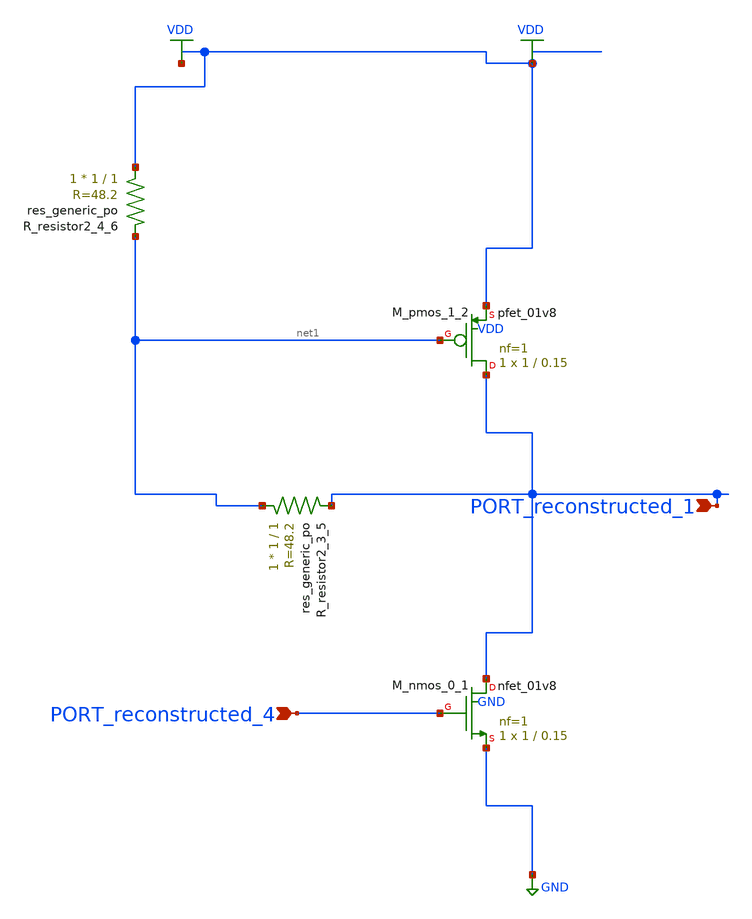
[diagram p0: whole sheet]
** sch_path: schematics/AMSNet/153.sch
**.subckt 153 PORT_reconstructed_1 PORT_reconstructed_4
*.ipin PORT_reconstructed_1
*.ipin PORT_reconstructed_4
XM_nmos_0_1 PORT_reconstructed_1 PORT_reconstructed_4 GND GND sky130_fd_pr__nfet_01v8 L=0.15 W=1 nf=1
+ ad='int((1 + 1)/2) * 1 / 1 * 0.29' as='int((1 + 2)/2) * 1 / 1 * 0.29' pd='2*int((1 + 1)/2) * (1 / 1 + 0.29)'
+ ps='2*int((1 + 2)/2) * (1 / 1 + 0.29)' nrd='0.29 / 1 ' nrs='0.29 / 1 ' sa=0 sb=0 sd=0 mult=1 m=1
XM_pmos_1_2 PORT_reconstructed_1 net1 VDD VDD sky130_fd_pr__pfet_01v8 L=0.15 W=1 nf=1 ad='int((1 + 1)/2) * 1 / 1 * 0.29'
+ as='int((1 + 2)/2) * 1 / 1 * 0.29' pd='2*int((1 + 1)/2) * (1 / 1 + 0.29)' ps='2*int((1 + 2)/2) * (1 / 1 + 0.29)'
+ nrd='0.29 / 1 ' nrs='0.29 / 1 ' sa=0 sb=0 sd=0 mult=1 m=1
XR_resistor2_3_5 net1 PORT_reconstructed_1 sky130_fd_pr__res_generic_po W=1 L=1 m=1
XR_resistor2_4_6 VDD net1 sky130_fd_pr__res_generic_po W=1 L=1 m=1
**.ends
.GLOBAL GND
.GLOBAL VDD
.end
